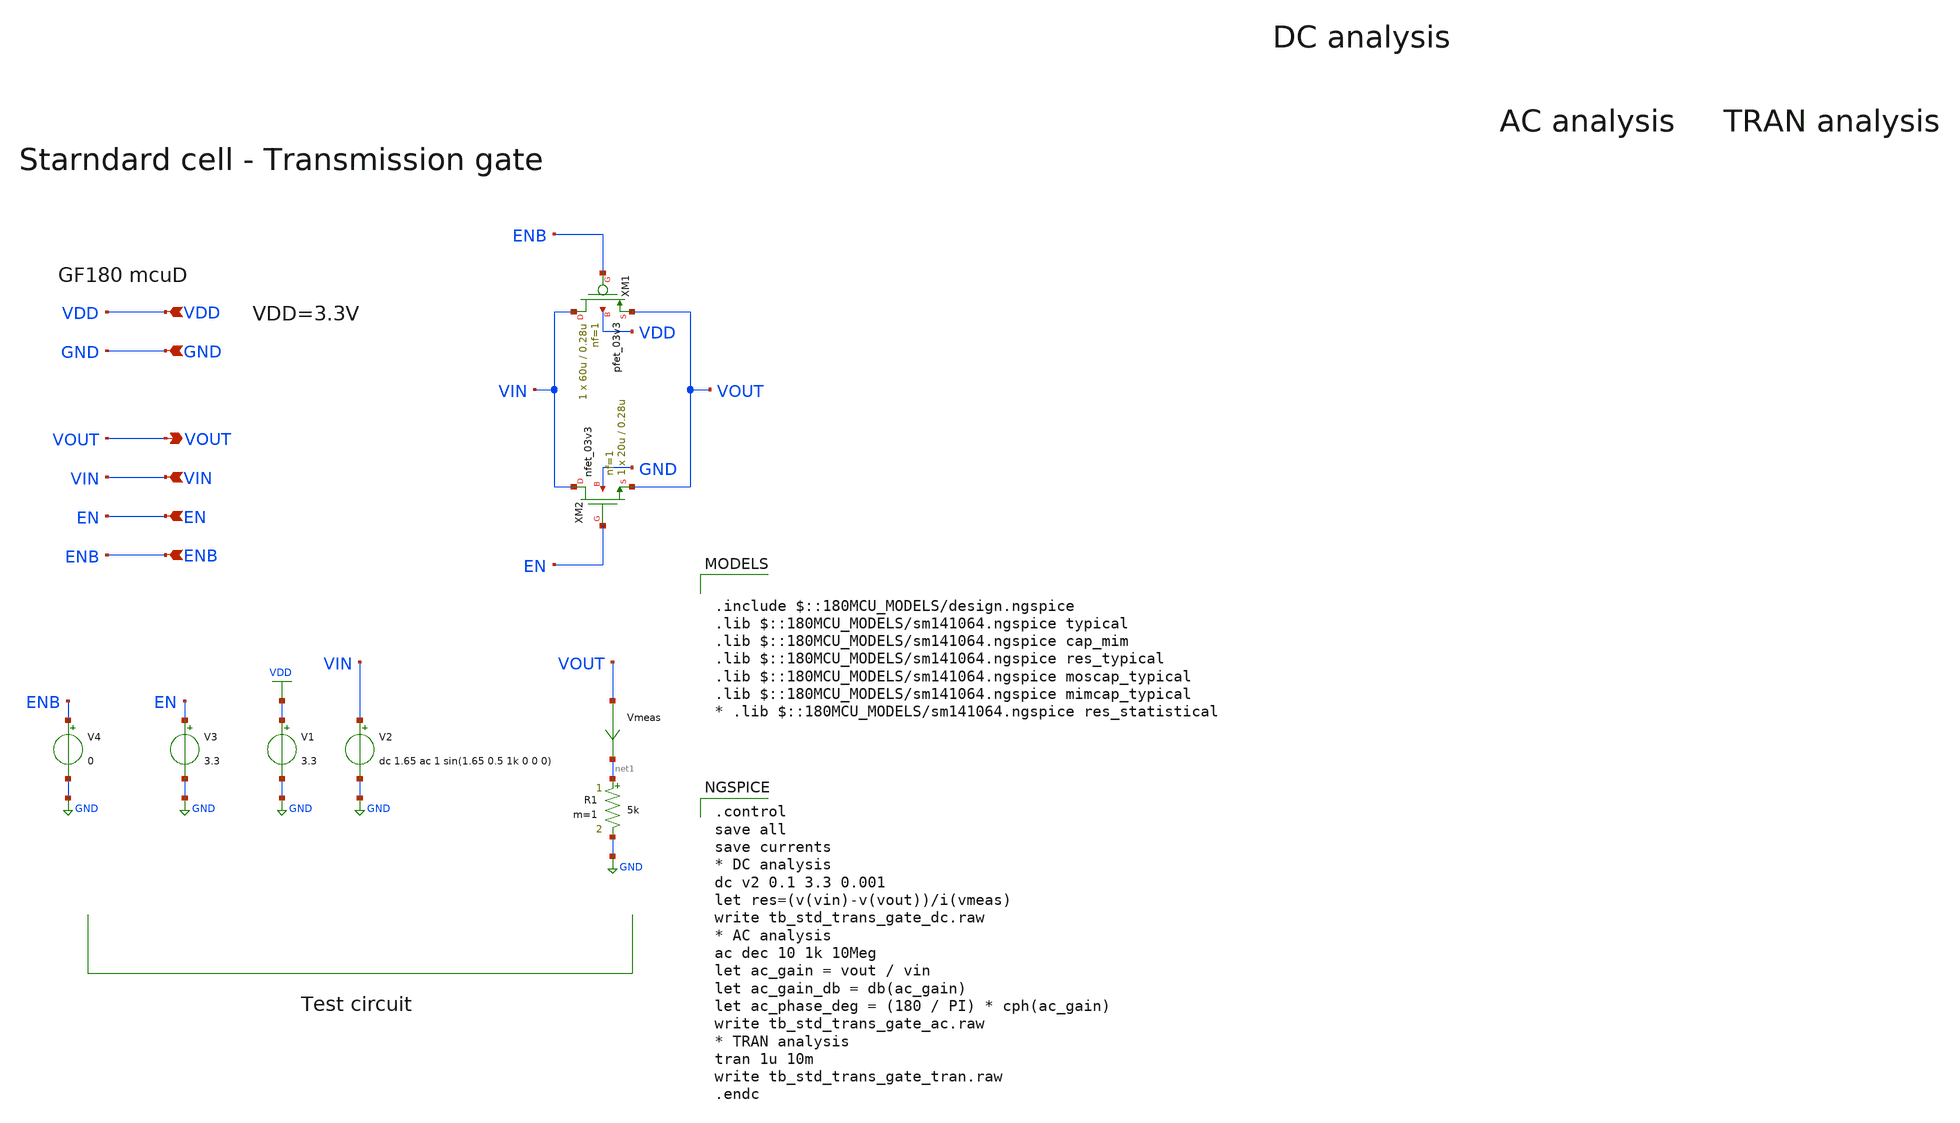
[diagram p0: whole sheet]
** sch_path: designs/libs/tb_analog/tb_trans_gate/tb_trans_gate.sch
* Copyright 2022 GlobalFoundries PDK Authors
* Licensed under the Apache License, Version 2.0 (the "License");
* you may not use this file except in compliance with the License.
* You may obtain a copy of the License at
* https://www.apache.org/licenses/LICENSE-2.0
* Unless required by applicable law or agreed to in writing, software
* distributed under the License is distributed on an "AS IS" BASIS,
* WITHOUT WARRANTIES OR CONDITIONS OF ANY KIND, either express or implied.
* See the License for the specific language governing permissions and
* limitations under the License.
**.subckt tb_trans_gate VDD GND VOUT VIN EN ENB
*.ipin VDD
*.ipin GND
*.opin VOUT
*.ipin VIN
*.ipin EN
*.ipin ENB
V1 VDD GND 3.3
V2 VIN GND dc 1.65 ac 1 sin(1.65 0.5 1k 0 0 0)
XM1 VIN ENB VOUT VDD pfet_03v3 L=0.28u W=60u nf=1 ad='int((nf+1)/2) * W/nf * 0.18u' as='int((nf+2)/2) * W/nf * 0.18u'
+ pd='2*int((nf+1)/2) * (W/nf + 0.18u)' ps='2*int((nf+2)/2) * (W/nf + 0.18u)' nrd='0.18u / W' nrs='0.18u / W'
+ sa=0 sb=0 sd=0 m=1
XM2 VIN EN VOUT GND nfet_03v3 L=0.28u W=20u nf=1 ad='int((nf+1)/2) * W/nf * 0.18u' as='int((nf+2)/2) * W/nf * 0.18u'
+ pd='2*int((nf+1)/2) * (W/nf + 0.18u)' ps='2*int((nf+2)/2) * (W/nf + 0.18u)' nrd='0.18u / W' nrs='0.18u / W'
+ sa=0 sb=0 sd=0 m=1
Vmeas VOUT net1 0
.save i(vmeas)
R1 net1 GND 5k m=1
V3 EN GND 3.3
V4 ENB GND 0
**** begin user architecture code

.control
save all
save currents
* DC analysis
dc v2 0.1 3.3 0.001
let res=(v(vin)-v(vout))/i(vmeas)
write tb_std_trans_gate_dc.raw
* AC analysis
ac dec 10 1k 10Meg
let ac_gain = vout / vin
let ac_gain_db = db(ac_gain)
let ac_phase_deg = (180 / PI) * cph(ac_gain)
write tb_std_trans_gate_ac.raw
* TRAN analysis
tran 1u 10m
write tb_std_trans_gate_tran.raw
.endc



.include $::180MCU_MODELS/design.ngspice
.lib $::180MCU_MODELS/sm141064.ngspice typical
.lib $::180MCU_MODELS/sm141064.ngspice cap_mim
.lib $::180MCU_MODELS/sm141064.ngspice res_typical
.lib $::180MCU_MODELS/sm141064.ngspice moscap_typical
.lib $::180MCU_MODELS/sm141064.ngspice mimcap_typical
* .lib $::180MCU_MODELS/sm141064.ngspice res_statistical

**** end user architecture code
**.ends
.GLOBAL VDD
.GLOBAL GND
.end
